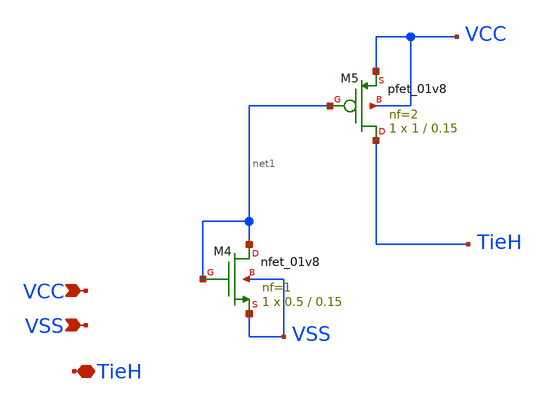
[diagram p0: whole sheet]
** sch_path: xschem/TieH_1p8.sch
**.subckt TieH_1p8 VCC VSS TieH
*.ipin VCC
*.ipin VSS
*.iopin TieH
XM4 net1 net1 VSS VSS sky130_fd_pr__nfet_01v8 L=0.15 W=0.5 nf=1 ad='int((nf+1)/2) * W/nf * 0.29' as='int((nf+2)/2) * W/nf * 0.29'
+ pd='2*int((nf+1)/2) * (W/nf + 0.29)' ps='2*int((nf+2)/2) * (W/nf + 0.29)' nrd='0.29 / W' nrs='0.29 / W'
+ sa=0 sb=0 sd=0 mult=1 m=1
XM5 TieH net1 VCC VCC sky130_fd_pr__pfet_01v8 L=0.15 W=1 nf=2 ad='int((nf+1)/2) * W/nf * 0.29' as='int((nf+2)/2) * W/nf * 0.29'
+ pd='2*int((nf+1)/2) * (W/nf + 0.29)' ps='2*int((nf+2)/2) * (W/nf + 0.29)' nrd='0.29 / W' nrs='0.29 / W'
+ sa=0 sb=0 sd=0 mult=1 m=1
**.ends
.end
